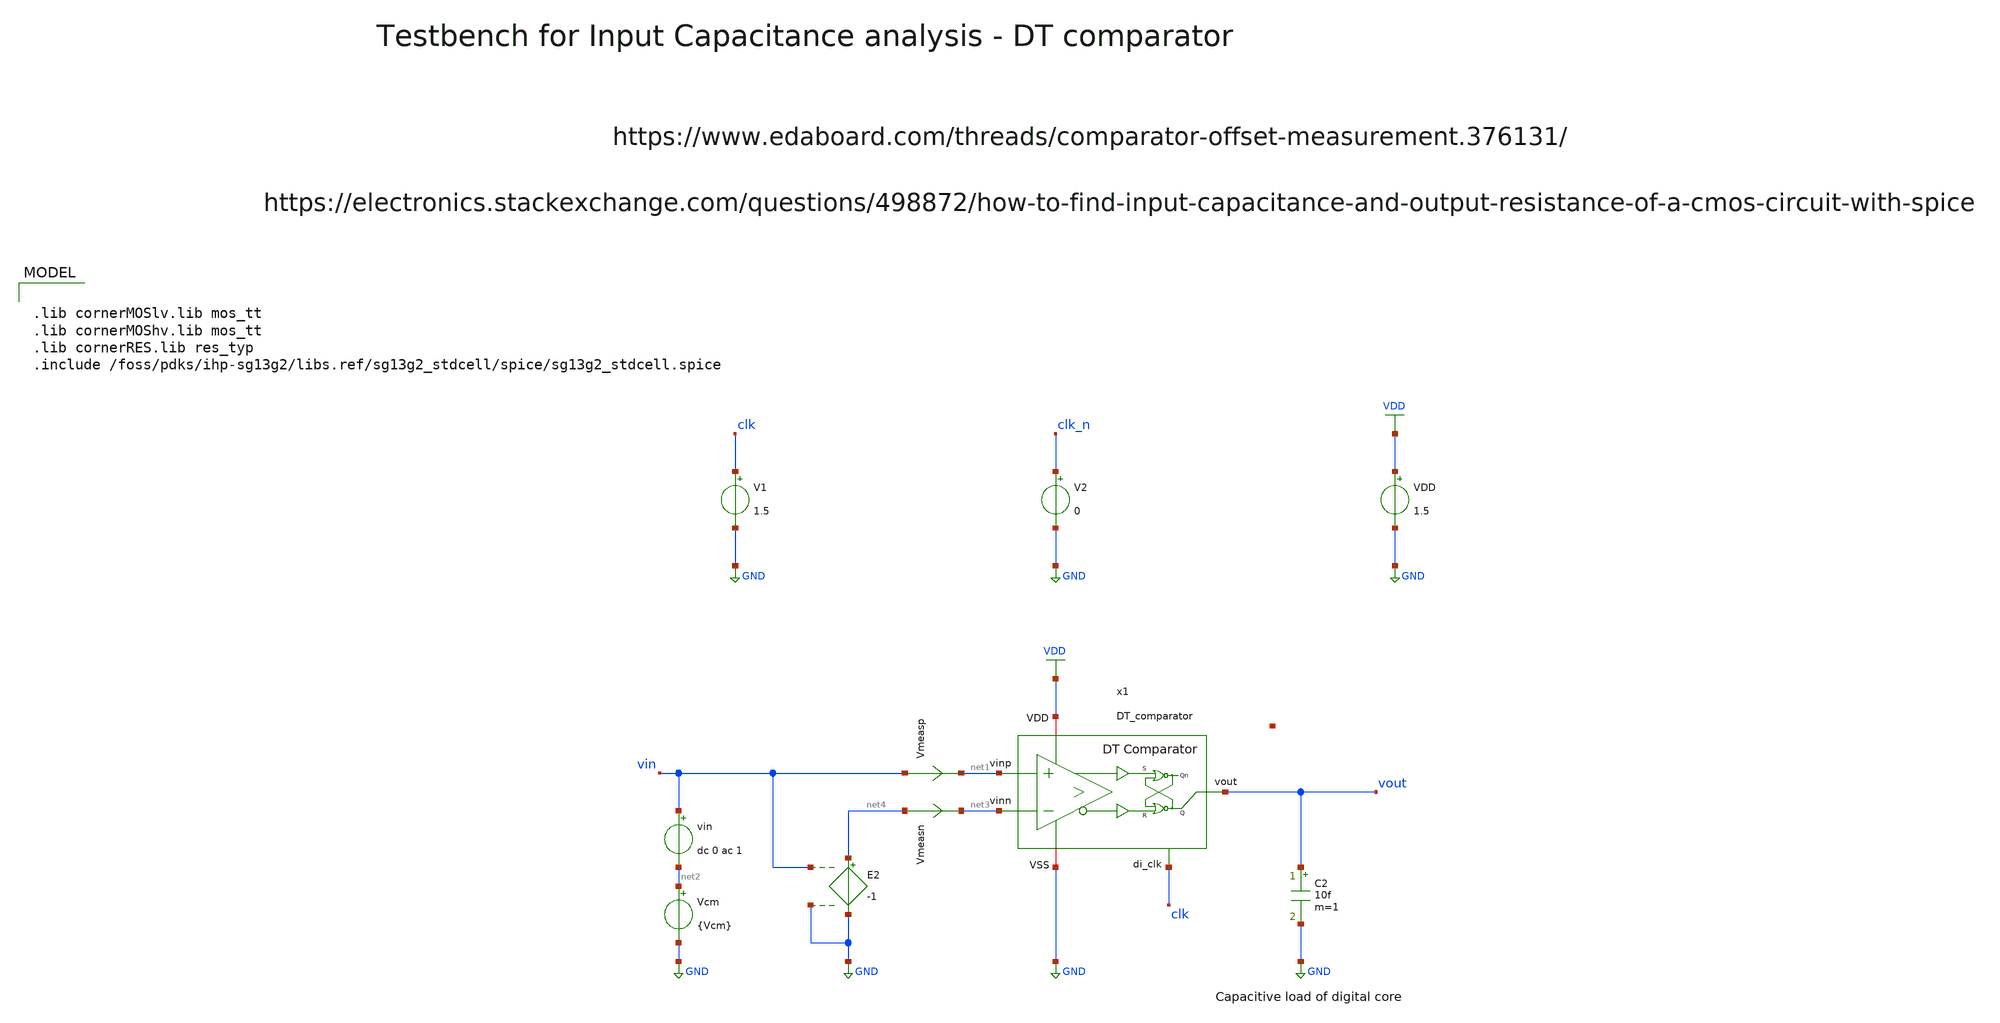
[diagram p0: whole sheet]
** sch_path: xschem/comparator/discrete_time/testbenches/DT_comparator_tb_ac_cin.sch
**.subckt DT_comparator_tb_ac_cin
VDD VDD GND 1.5
V1 clk GND 1.5
V2 clk_n GND 0
Vmeasp vin net1 0
.save i(vmeasp)
Vmeasn net4 net3 0
.save i(vmeasn)
vin vin net2 dc 0 ac 1
Vcm net2 GND {Vcm}
E2 net4 GND vin GND -1
C2 vout GND 10f m=1
x1 VDD net1 vout net3 clk GND net5 DT_comparator
**** begin user architecture code

.lib cornerMOSlv.lib mos_tt
.lib cornerMOShv.lib mos_tt
.lib cornerRES.lib res_typ
.include /foss/pdks/ihp-sg13g2/libs.ref/sg13g2_stdcell/spice/sg13g2_stdcell.spice



.param temp=27
.param Vcm=0.75
.options savecurrents reltol=1e-3 abstol=1e-12 gmin=1e-15
.control
save all

* User Constants
let fstart = 1
let fstop = 1G

* Operating Point Analysis
op
remzerovec
write DT_comparator_tb_ac_cin.raw
* set appendwrite

* AC Analysis
ac dec 101 $&fstart $&fstop
remzerovec
write DT_comparator_tb_ac_cin.raw

* Plotting Cinp
let Cinp = mag(i(Vmeasp)) / (2 * 3.14 * frequency)
plot Cinp

* Plotting Cinn
let Cinn = mag(i(Vmeasn)) / (2 * 3.14 * frequency)
plot Cinn

* Measure avg. Cinp & Cinn
meas ac Cinp_avg AVG Cinp from=fstart to=fstop
meas ac Cinn_avg AVG Cinn from=fstart to=fstop

* Writing Data
set wr_singlescale
set wr_vecnames
wrdata /foss/designs/SG13G2_ATBS-ADC-main/python/plot_simulations/data/DT_comparator_tb_ac_cin.txt
+ v(Cinp) v(Cinn)

*quit
.endc

**** end user architecture code
**.ends
.GLOBAL GND
.GLOBAL VDD
.end
